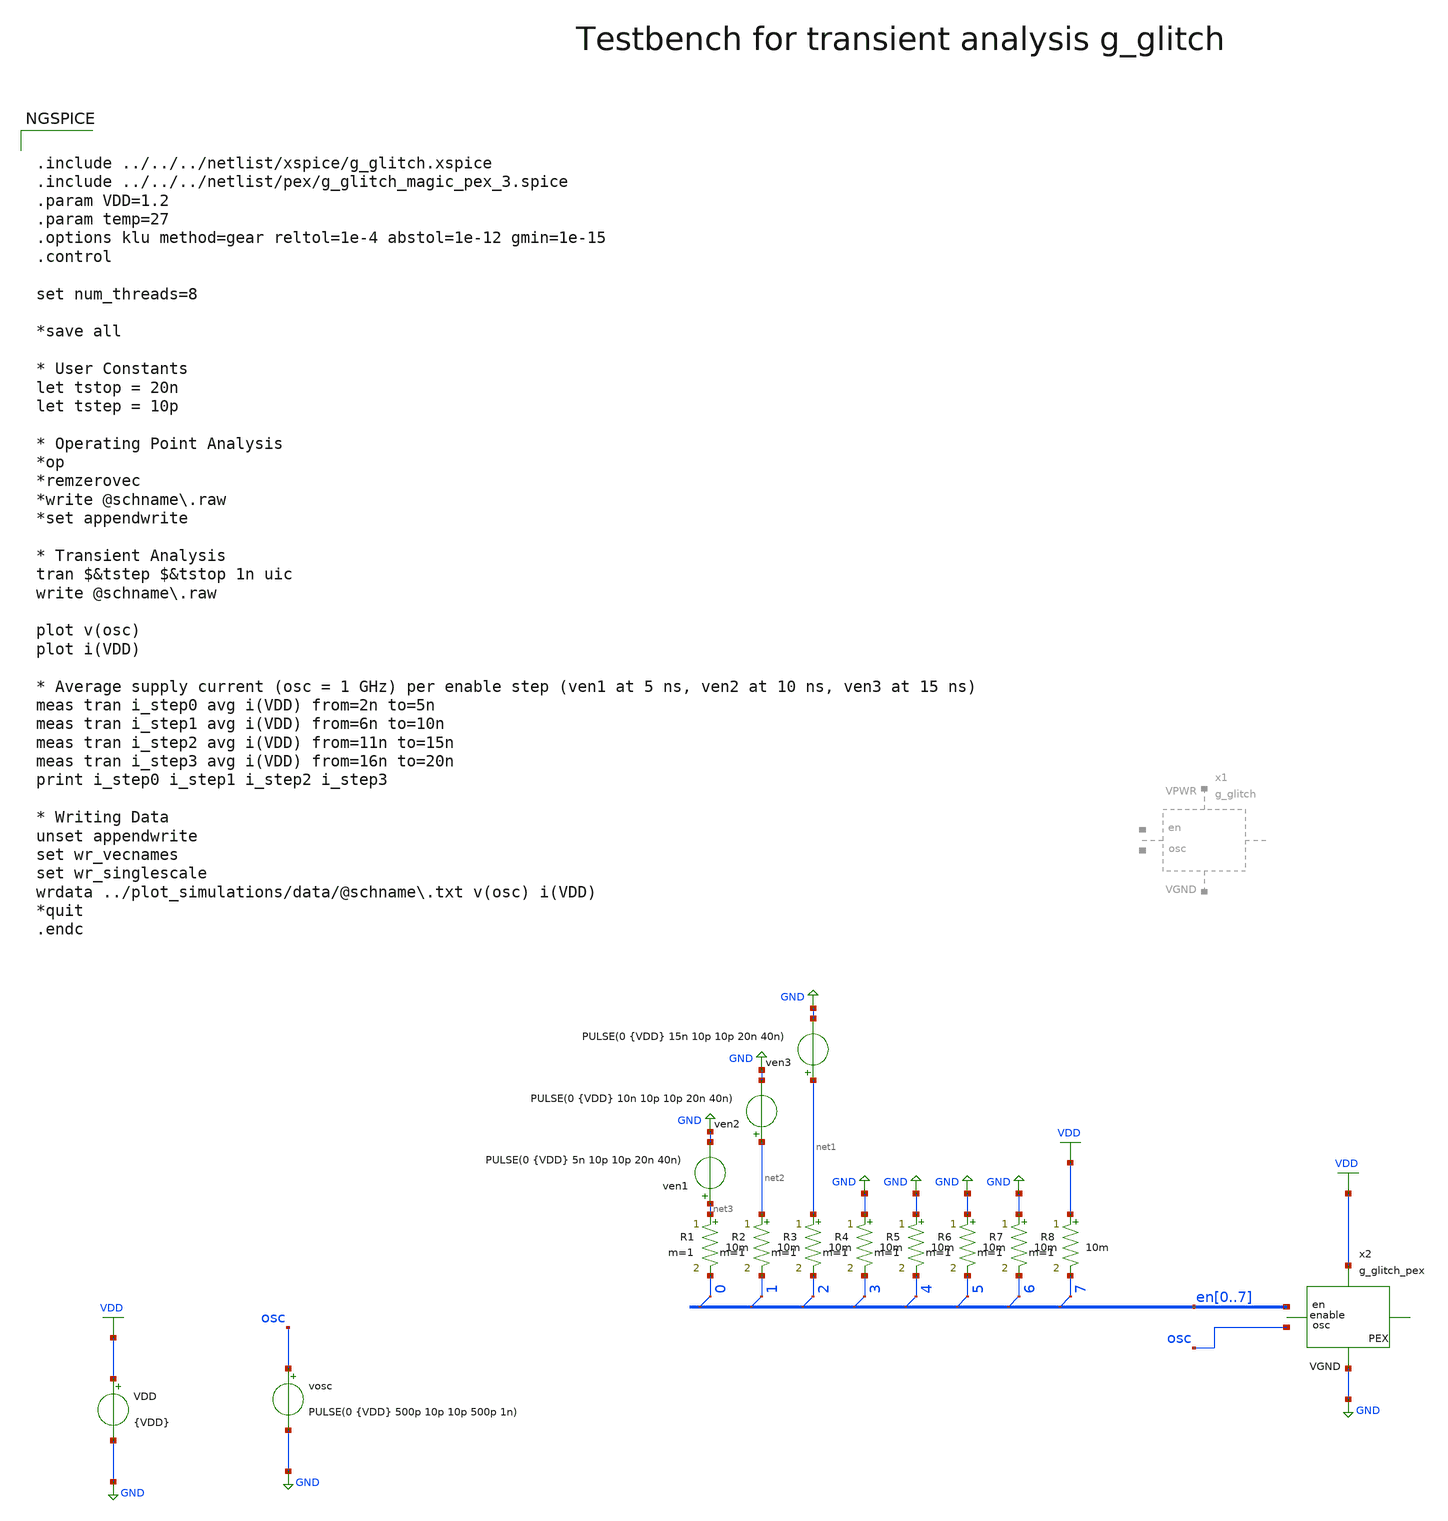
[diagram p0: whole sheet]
** sch_path: macros/heichips26_digital_project/macros/g_glitch/testbenches/xschem/g_glitch_tb_tran.sch
**.subckt g_glitch_tb_tran
VDD VDD GND {VDD}
ven1 net3 GND PULSE(0 {VDD} 5n 10p 10p 20n 40n)
x2 VDD GND osc en0 en1 en2 en3 en4 en5 en6 en7 g_glitch_pex
* tap: en[0..7] --> en0
* tap: en[0..7] --> en2
* tap: en[0..7] --> en4
* tap: en[0..7] --> en6
* tap: en[0..7] --> en7
* tap: en[0..7] --> en5
* tap: en[0..7] --> en3
* tap: en[0..7] --> en1
R1 net3 en0 10m m=1
R2 net2 en1 10m m=1
R3 net1 en2 10m m=1
R4 GND en3 10m m=1
R5 GND en4 10m m=1
R6 GND en5 10m m=1
R7 GND en6 10m m=1
R8 VDD en7 10m m=1
ven2 net2 GND PULSE(0 {VDD} 10n 10p 10p 20n 40n)
ven3 net1 GND PULSE(0 {VDD} 15n 10p 10p 20n 40n)
vosc osc GND PULSE(0 {VDD} 500p 10p 10p 500p 1n)
**** begin user architecture code


.include ../../../netlist/xspice/g_glitch.xspice
.include ../../../netlist/pex/g_glitch_magic_pex_3.spice
.param VDD=1.2
.param temp=27
.options klu method=gear reltol=1e-4 abstol=1e-12 gmin=1e-15
.control

set num_threads=8

*save all

* User Constants
let tstop = 20n
let tstep = 10p

* Operating Point Analysis
*op
*remzerovec
*write @schname\.raw
*set appendwrite

* Transient Analysis
tran $&tstep $&tstop 1n uic
write @schname\.raw

plot v(osc)
plot i(VDD)

* Average supply current (osc = 1 GHz) per enable step (ven1 at 5 ns, ven2 at 10 ns, ven3 at 15 ns)
meas tran i_step0 avg i(VDD) from=2n to=5n
meas tran i_step1 avg i(VDD) from=6n to=10n
meas tran i_step2 avg i(VDD) from=11n to=15n
meas tran i_step3 avg i(VDD) from=16n to=20n
print i_step0 i_step1 i_step2 i_step3

* Writing Data
unset appendwrite
set wr_vecnames
set wr_singlescale
wrdata ../plot_simulations/data/@schname\.txt v(osc) i(VDD)
*quit
.endc


.lib cornerMOSlv.lib mos_tt
.lib cornerMOShv.lib mos_tt
.lib cornerRES.lib res_typ
.lib cornerDIO.lib dio_tt

**** end user architecture code
**.ends
.GLOBAL GND
.GLOBAL VDD
.end
